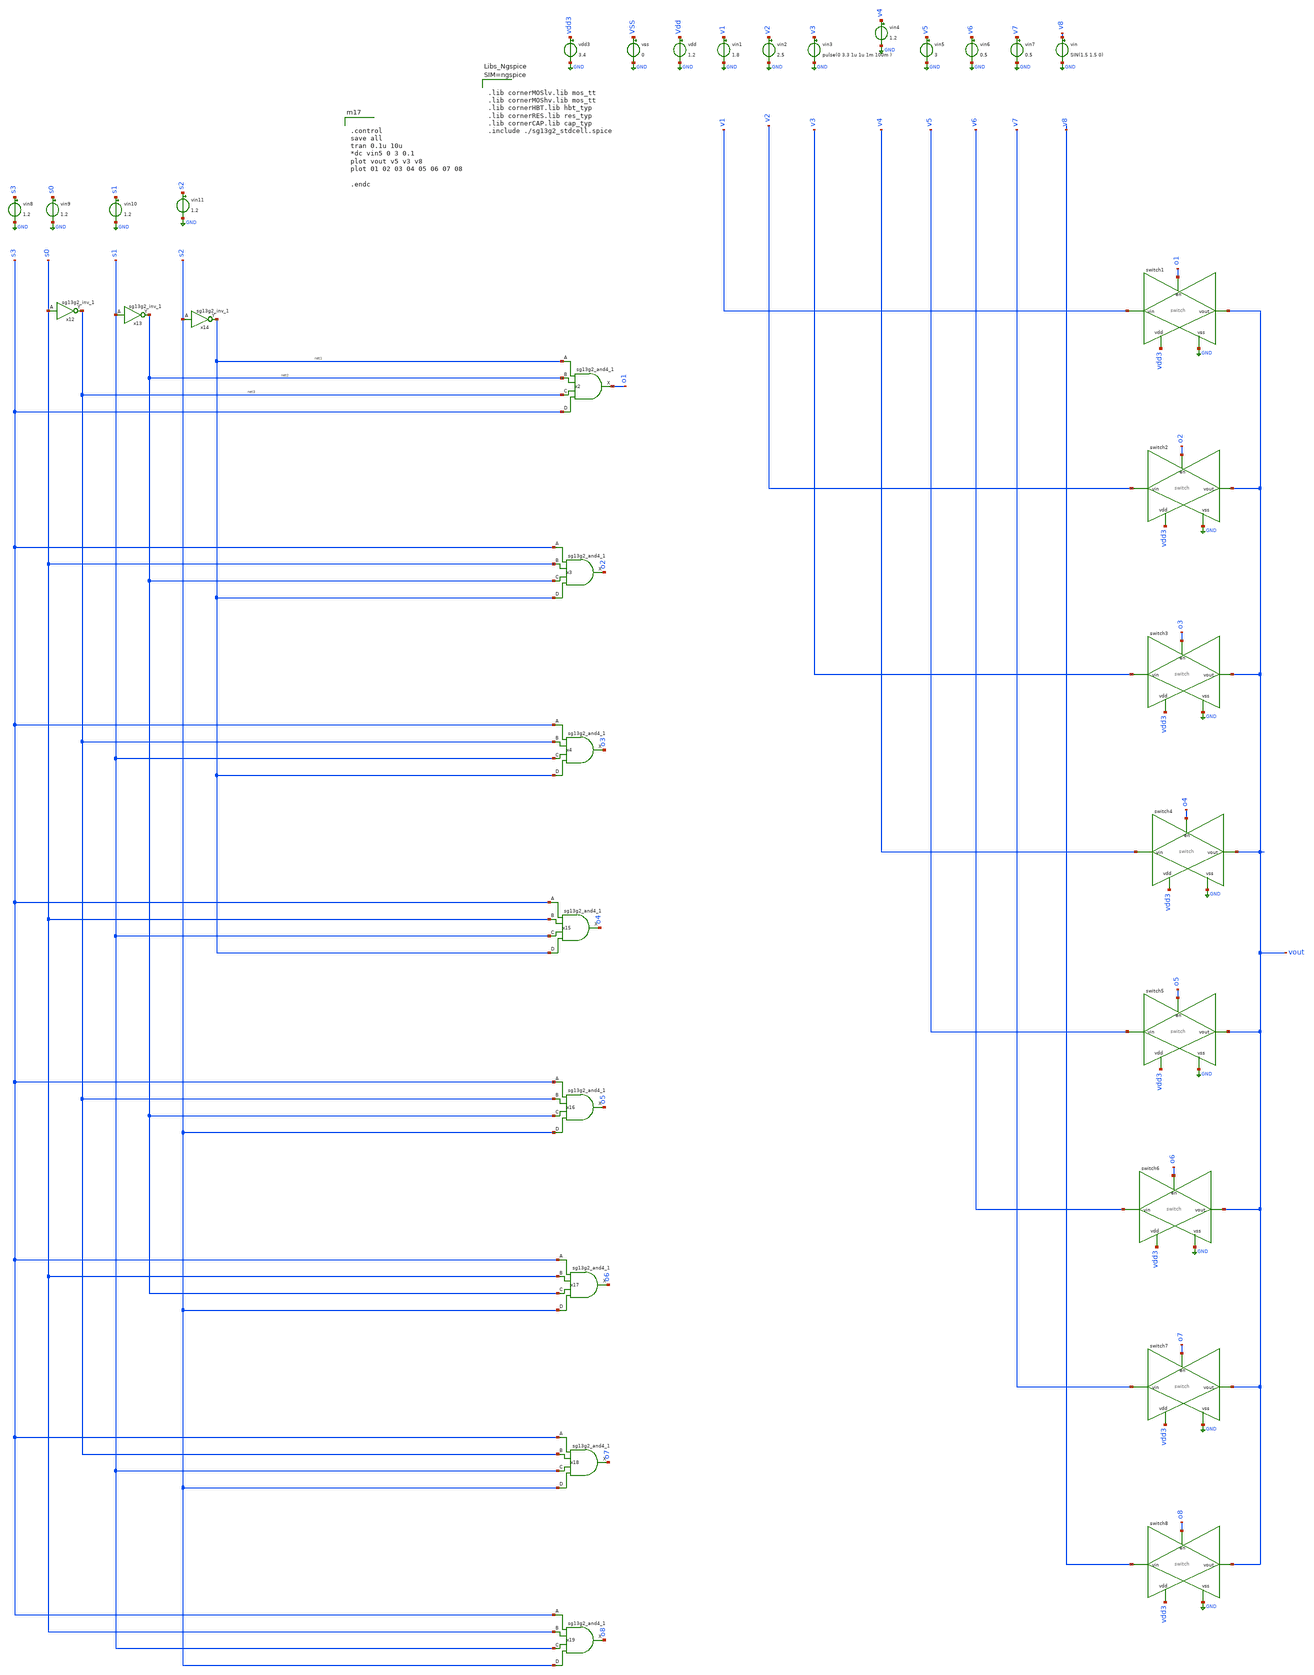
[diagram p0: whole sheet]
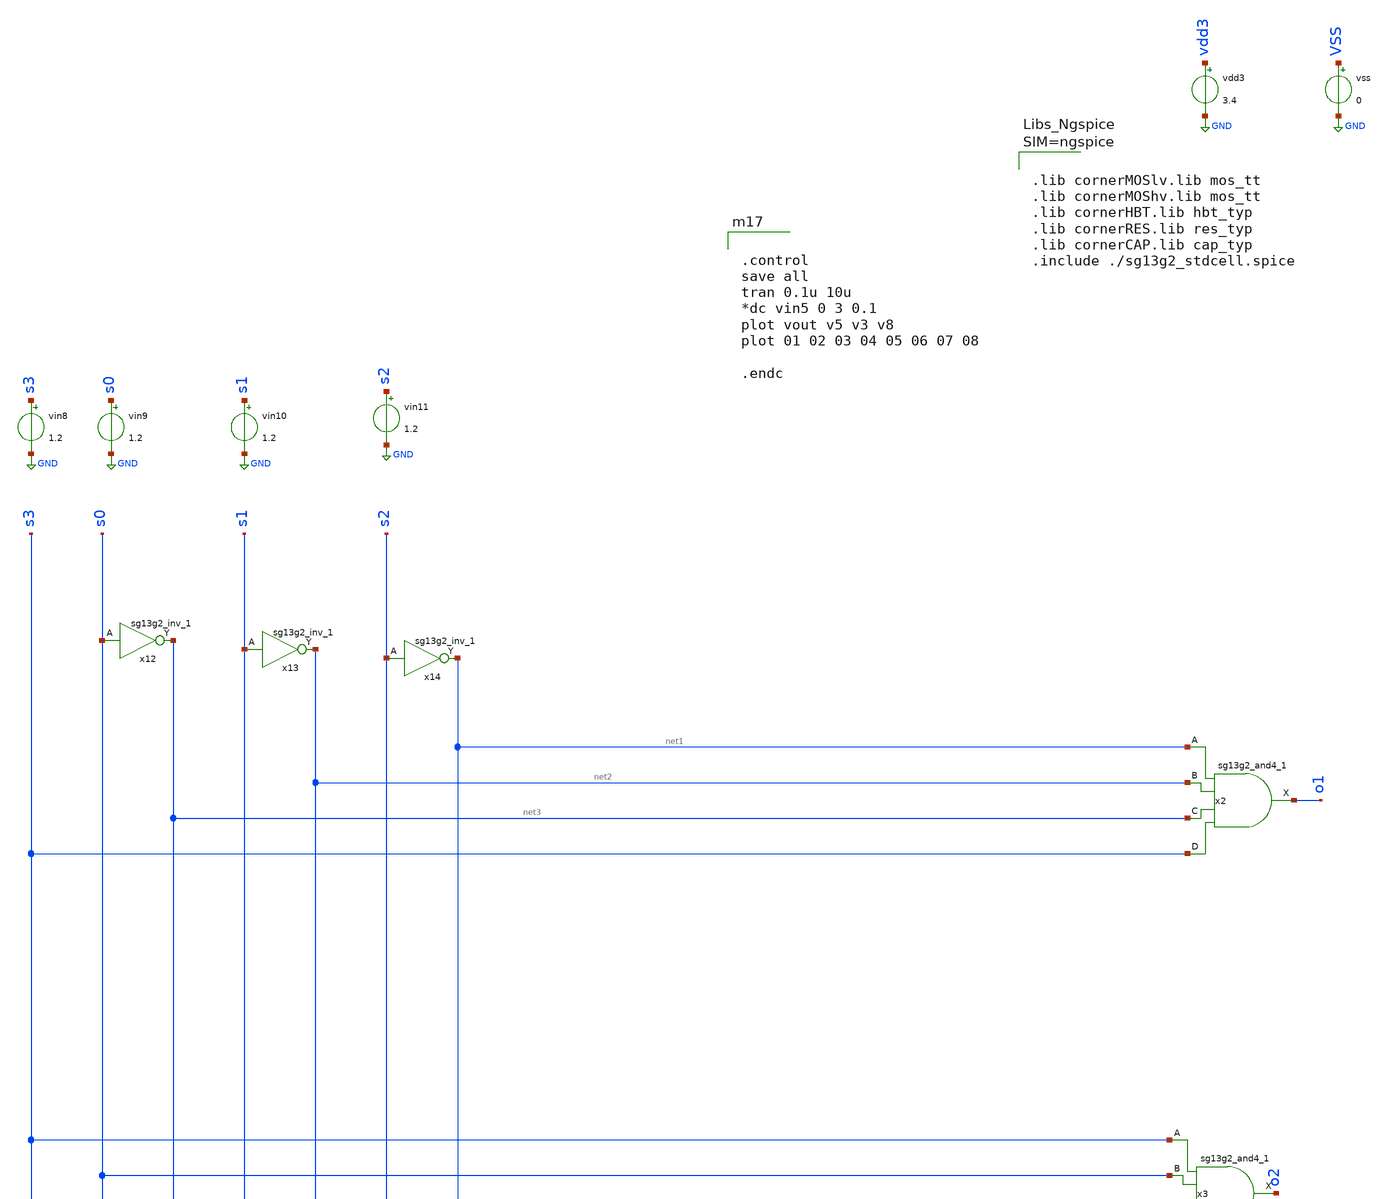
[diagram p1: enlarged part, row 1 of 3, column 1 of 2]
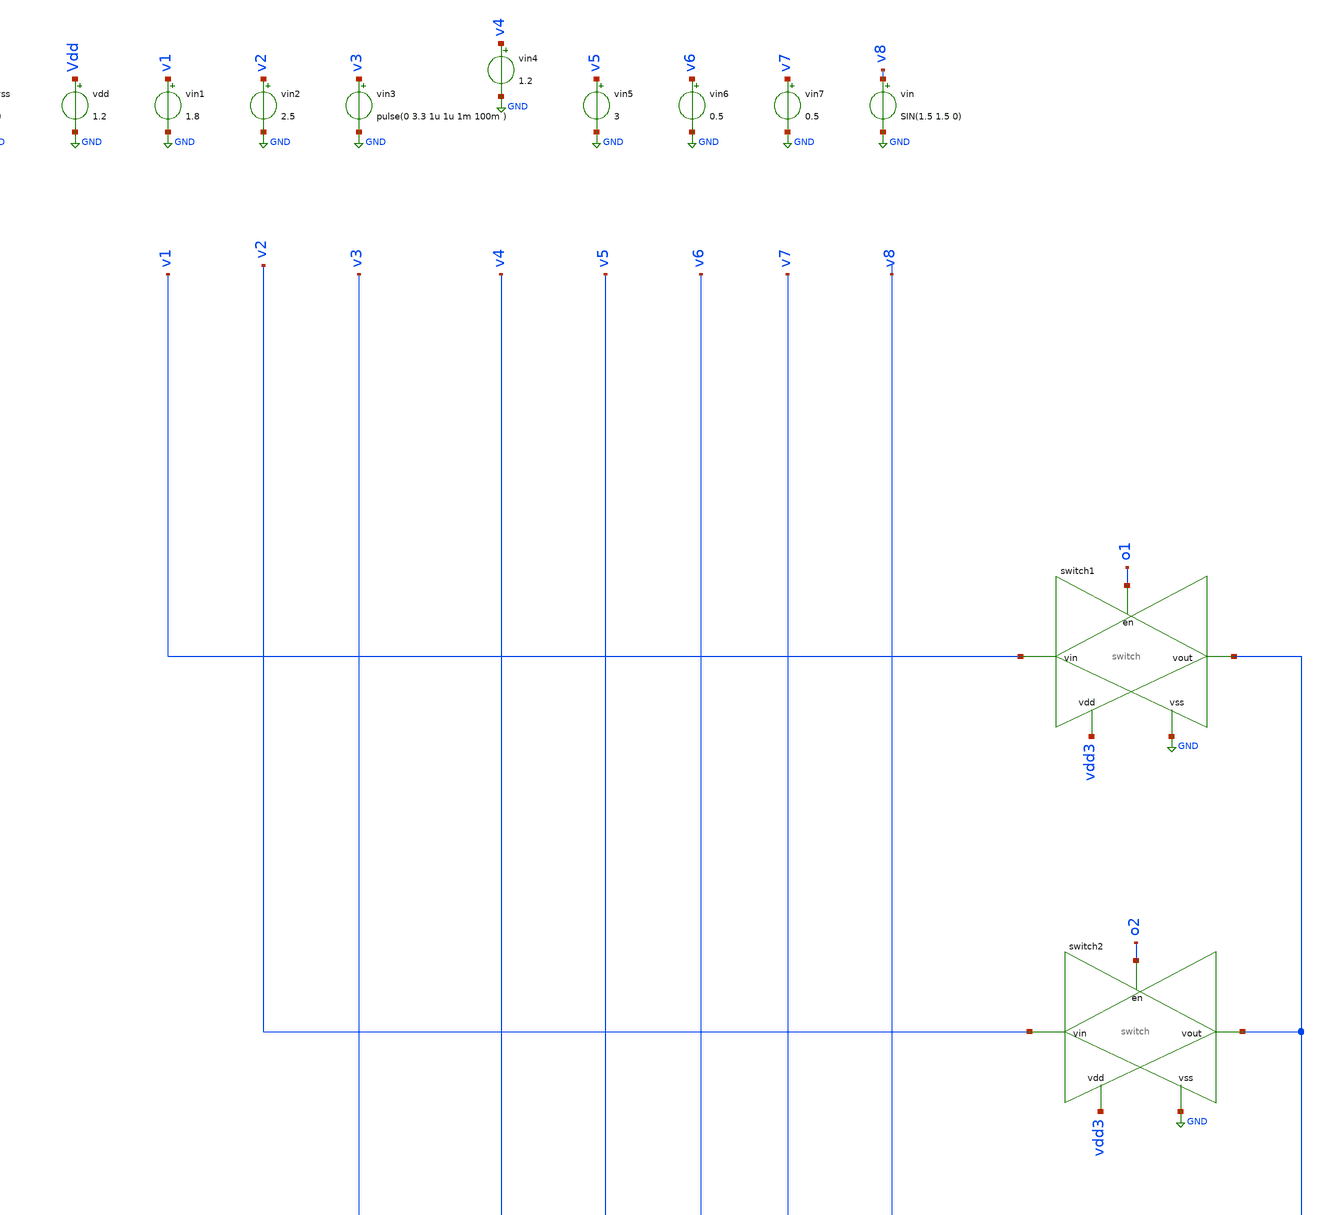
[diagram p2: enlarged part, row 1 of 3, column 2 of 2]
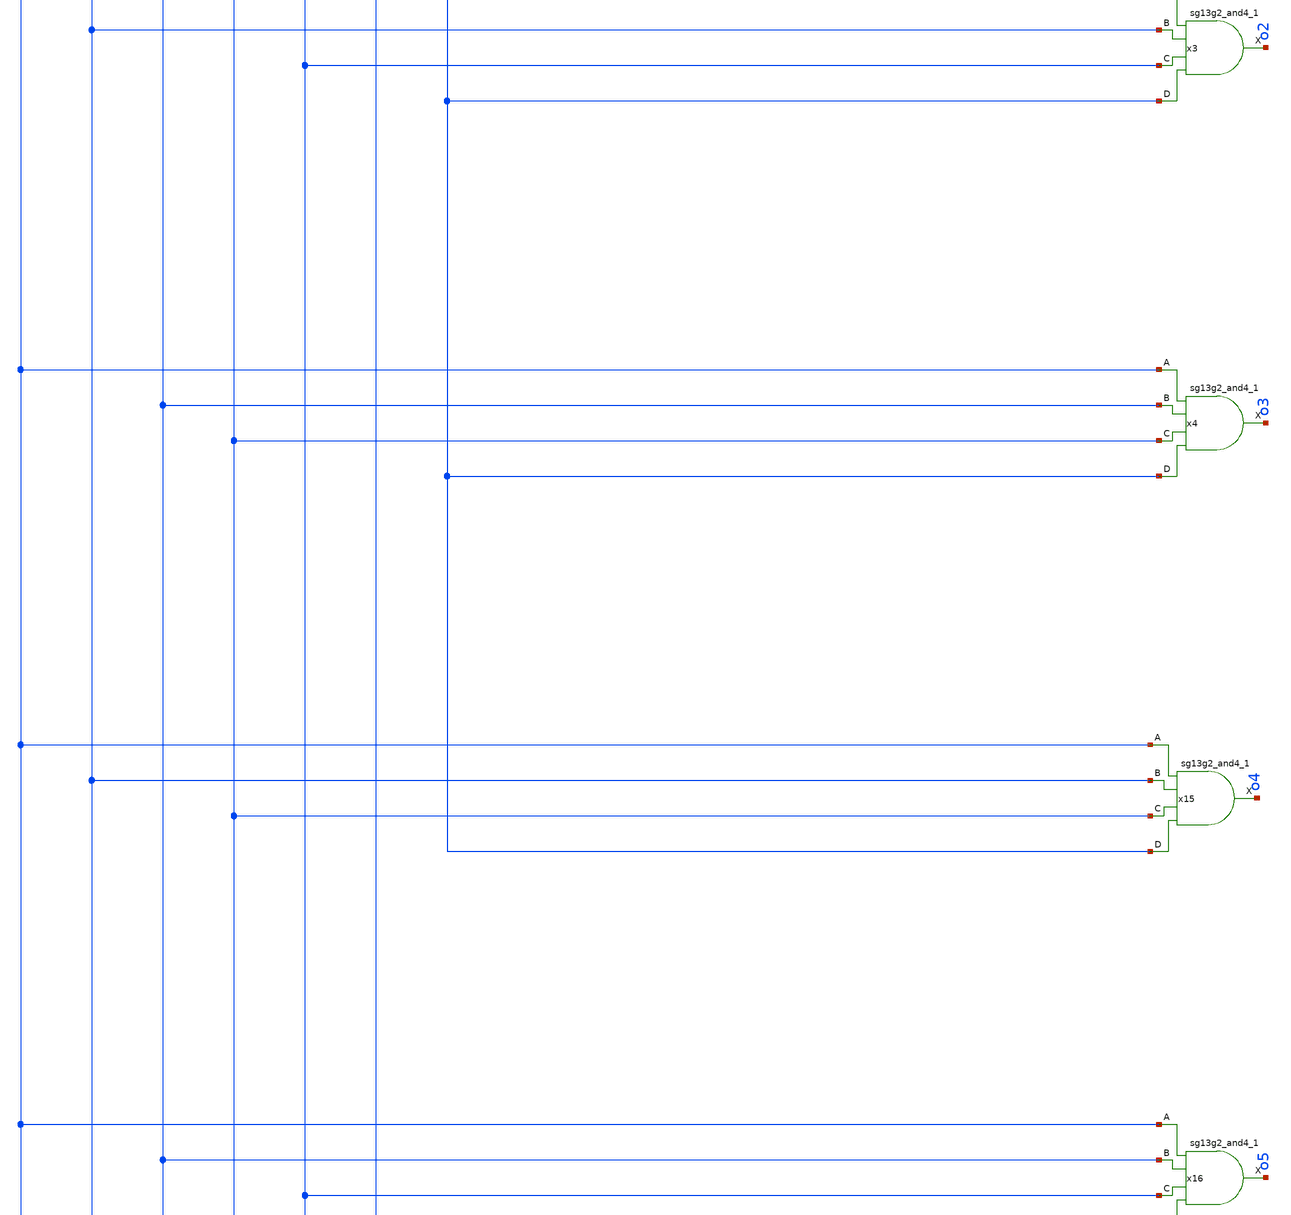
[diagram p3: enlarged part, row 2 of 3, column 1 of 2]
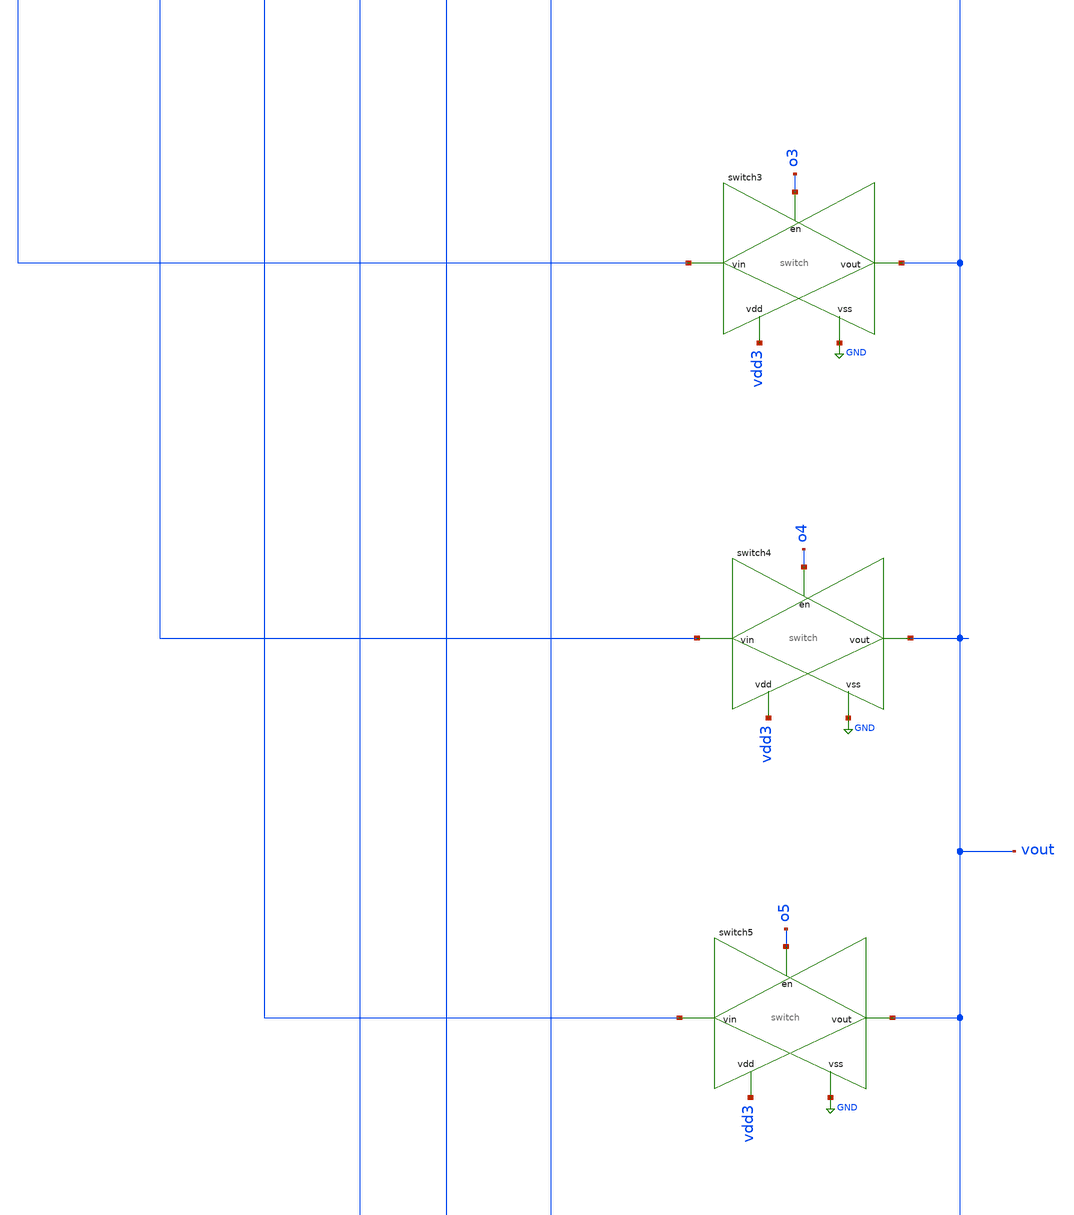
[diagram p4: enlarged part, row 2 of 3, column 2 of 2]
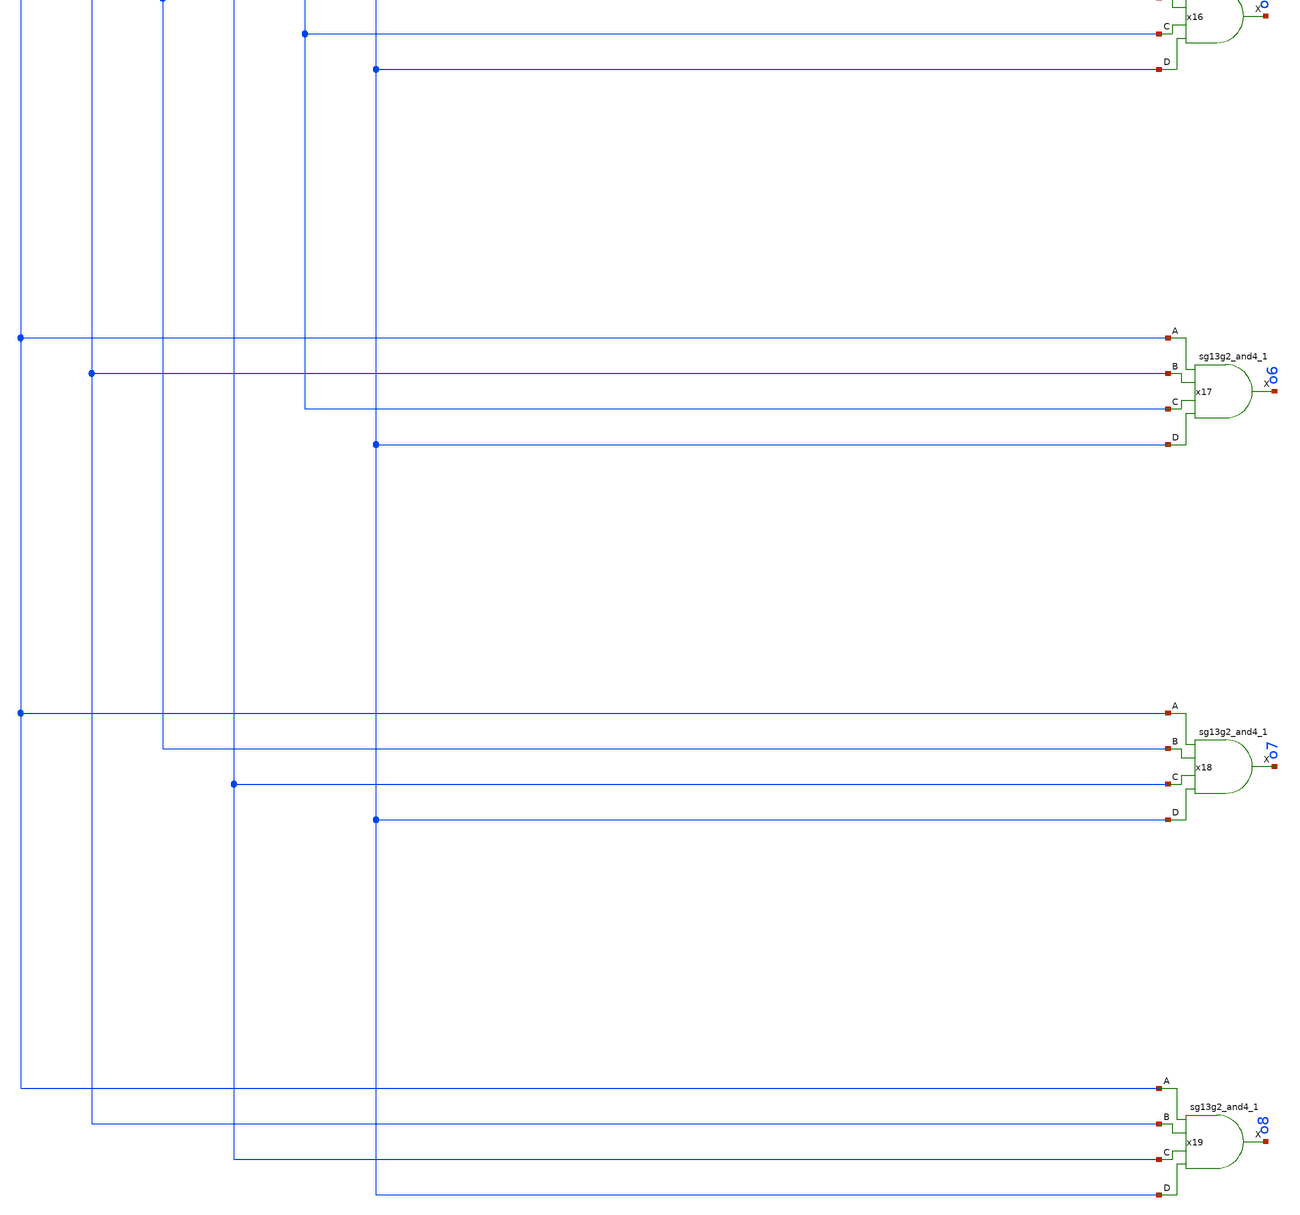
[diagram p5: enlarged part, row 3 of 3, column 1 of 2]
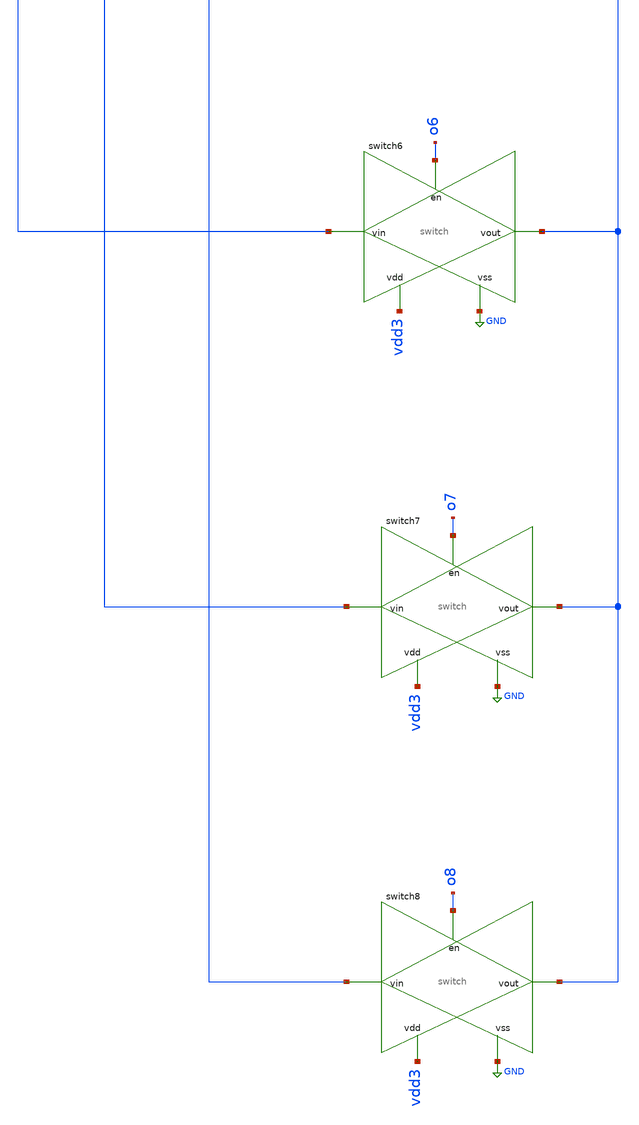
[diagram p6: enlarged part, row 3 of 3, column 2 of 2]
** sch_path: dependencies/DFT/DFT-main/schematic/xschem/schematique/block de test.sch
**.subckt block de test
x12 net3 s0 VDD VSS sg13g2_inv_1
x13 net2 s1 VDD VSS sg13g2_inv_1
x14 net1 s2 VDD VSS sg13g2_inv_1
x2 o1 net1 net2 net3 s3 VDD VSS sg13g2_and4_1
x3 o2 s3 s0 net2 net1 VDD VSS sg13g2_and4_1
x4 o3 s3 net3 s1 net1 VDD VSS sg13g2_and4_1
x15 o4 s3 s0 s1 net1 VDD VSS sg13g2_and4_1
x16 o5 s3 net3 net2 s2 VDD VSS sg13g2_and4_1
x17 o6 s3 s0 net2 s2 VDD VSS sg13g2_and4_1
x18 o7 s3 net3 s1 s2 VDD VSS sg13g2_and4_1
x19 o8 s3 s0 s1 s2 VDD VSS sg13g2_and4_1
vin v8 GND SIN(1.5 1.5 0)
vin1 v1 GND 1.8
vin2 v2 GND 2.5
vin3 v3 GND pulse(0 3.3 1u 1u 1m 100m )
vin4 v4 GND 1.2
vin5 v5 GND 3
vin6 v6 GND 0.5
vin7 v7 GND 0.5
vin8 s3 GND 1.2
vin9 s0 GND 1.2
vin10 s1 GND 1.2
vin11 s2 GND 1.2
xswitch1 o1 v1 vout GND vdd3 switch
vdd Vdd GND 1.2
xswitch2 o2 v2 vout GND vdd3 switch
xswitch3 o3 v3 vout GND vdd3 switch
xswitch4 o4 v4 vout GND vdd3 switch
xswitch5 o5 v5 vout GND vdd3 switch
xswitch6 o6 v6 vout GND vdd3 switch
xswitch7 o7 v7 vout GND vdd3 switch
xswitch8 o8 v8 vout GND vdd3 switch
vss VSS GND 0
vdd3 vdd3 GND 3.4
**** begin user architecture code



.lib cornerMOSlv.lib mos_tt
.lib cornerMOShv.lib mos_tt
.lib cornerHBT.lib hbt_typ
.lib cornerRES.lib res_typ
.lib cornerCAP.lib cap_typ
.include ./sg13g2_stdcell.spice





.control
save all
tran 0.1u 10u
*dc vin5 0 3 0.1
plot vout v5 v3 v8
plot 01 02 03 04 05 06 07 08

.endc

**** end user architecture code
**.ends

* expanding   symbol:  sg13g2_stdcells/sg13g2_inv_1.sym # of pins=2
** sym_path: sg13g2_stdcells/sg13g2_inv_1.sym
** sch_path: sg13g2_stdcells/sg13g2_inv_1.sch
.subckt sg13g2_inv_1 Y A VDD VSS
*.opin Y
*.ipin A
*.iopin VDD
*.iopin VSS
XM1 Y A VSS VSS sg13_lv_nmos w=740.00n l=130.00n ng=1 m=1 mm_ok=1
XM2 Y A VDD VDD sg13_lv_pmos w=1.12u l=130.00n ng=1 m=1 mm_ok=1
.ends


* expanding   symbol:  sg13g2_stdcells/sg13g2_and4_1.sym # of pins=5
** sym_path: sg13g2_stdcells/sg13g2_and4_1.sym
** sch_path: sg13g2_stdcells/sg13g2_and4_1.sch
.subckt sg13g2_and4_1 X A B C D VDD VSS
*.ipin A
*.ipin B
*.ipin C
*.ipin D
*.opin X
*.iopin VDD
*.iopin VSS
XM1 net1 A net3 VSS sg13_lv_nmos w=640.00n l=130.00n ng=1 m=1 mm_ok=1
XM2 net3 B net2 VSS sg13_lv_nmos w=640.00n l=130.00n ng=1 m=1 mm_ok=1
XM3 net2 C net4 VSS sg13_lv_nmos w=640.00n l=130.00n ng=1 m=1 mm_ok=1
XM4 net4 D VSS VSS sg13_lv_nmos w=640.00n l=130.00n ng=1 m=1 mm_ok=1
XM5 X net1 VSS VSS sg13_lv_nmos w=740.00n l=130.00n ng=1 m=1 mm_ok=1
XM6 net1 D VDD VDD sg13_lv_pmos w=840.00n l=130.00n ng=1 m=1 mm_ok=1
XM7 net1 C VDD VDD sg13_lv_pmos w=840.00n l=130.00n ng=1 m=1 mm_ok=1
XM8 net1 B VDD VDD sg13_lv_pmos w=840.00n l=130.00n ng=1 m=1 mm_ok=1
XM9 net1 A VDD VDD sg13_lv_pmos w=840.00n l=130.00n ng=1 m=1 mm_ok=1
XM10 X net1 VDD VDD sg13_lv_pmos w=1.12u l=130.00n ng=1 m=1 mm_ok=1
.ends


* expanding   symbol:  /foss/designs/simulations/switch.sym # of pins=5
** sym_path: dependencies/DFT/DFT-main/schematic/xschem/schematique/switch.sym
** sch_path: dependencies/DFT/DFT-main/schematic/xschem/schematique/switch.sch
.subckt switch en vin vout vss vdd
*.iopin vin
*.iopin vout
*.ipin en
*.iopin vss
*.iopin vdd
XM5 en_n en vdd vdd sg13_hv_pmos w=0.3u l=0.4u ng=1 m=1 mm_ok=1
XM6 en_n en vss vss sg13_hv_nmos w=2u l=0.45u ng=1 m=1 mm_ok=1
XM7 en_3 en_n vdd vdd sg13_hv_pmos w=0.3u l=0.4u ng=1 m=1 mm_ok=1
XM8 en_3 en_n vss vss sg13_hv_nmos w=0.3u l=0.45u ng=1 m=1 mm_ok=1
XM1 vout en_3 vin vss sg13_hv_nmos w=4u l=0.45u ng=1 m=1 mm_ok=1
XM2 vout en_n vin vdd sg13_hv_pmos w=10u l=0.45u ng=1 m=1 mm_ok=1
.ends

.GLOBAL GND
.end
